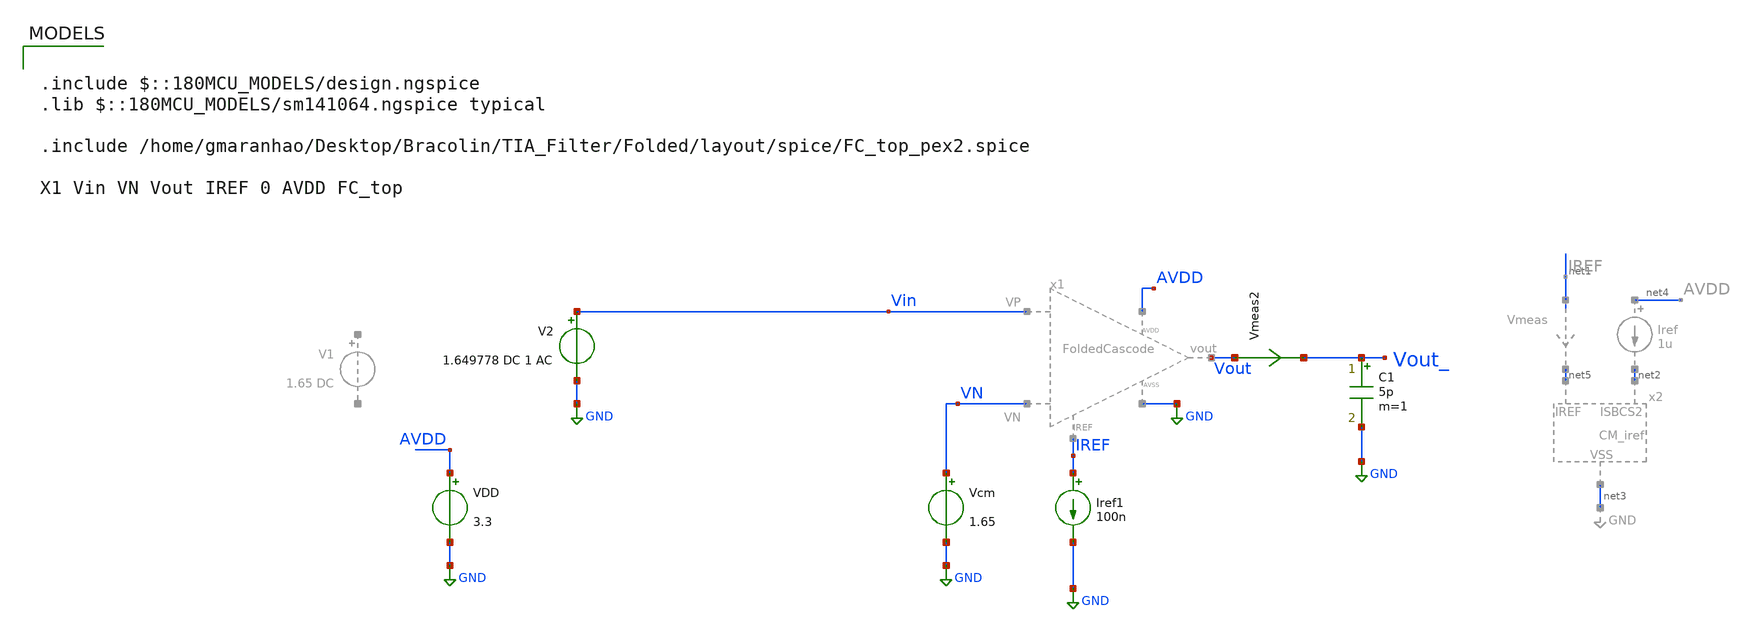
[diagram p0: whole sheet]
** sch_path: TIA_Filter/Folded/TB_Folded_dc.sch
**.subckt TB_Folded_dc
VDD AVDD GND 3.3
Vcm VN GND 1.65
Vmeas2 Vout Vout_ 0
.save i(vmeas2)
C1 Vout_ GND 5p m=1
Iref1 IREF GND 100n
V2 Vin GND 1.649778 DC 1 AC
**** begin user architecture code

.include $::180MCU_MODELS/design.ngspice
.lib $::180MCU_MODELS/sm141064.ngspice typical

.include /home/gmaranhao/Desktop/Bracolin/TIA_Filter/Folded/layout/spice/FC_top_pex2.spice

X1 Vin VN Vout IREF 0 AVDD FC_top



.option gmin=1e-18



.control
save all

*set temp=80

op
remzerovec
write TB_Folded_dc.raw
set appendwrite

*dc V2 1.648 1.651 0.001m
*remzerovec
*write TB_Folded_dc.raw
*wrdata /home/gmaranhao/Desktop/Bracolin/TIA_Filter/Folded/plots/DC-AC/Folded_DC_100n_PEX.txt
*+ V(Vout)



ac dec 10 1m 1e9
remzerovec
write TB_Folded_dc.raw
wrdata /home/gmaranhao/Desktop/Bracolin/TIA_Filter/Folded/plots/DC-AC/Folded_AC_100n_PEX.txt V(Vout)


.endc


**** end user architecture code
**.ends
.GLOBAL GND
.end
